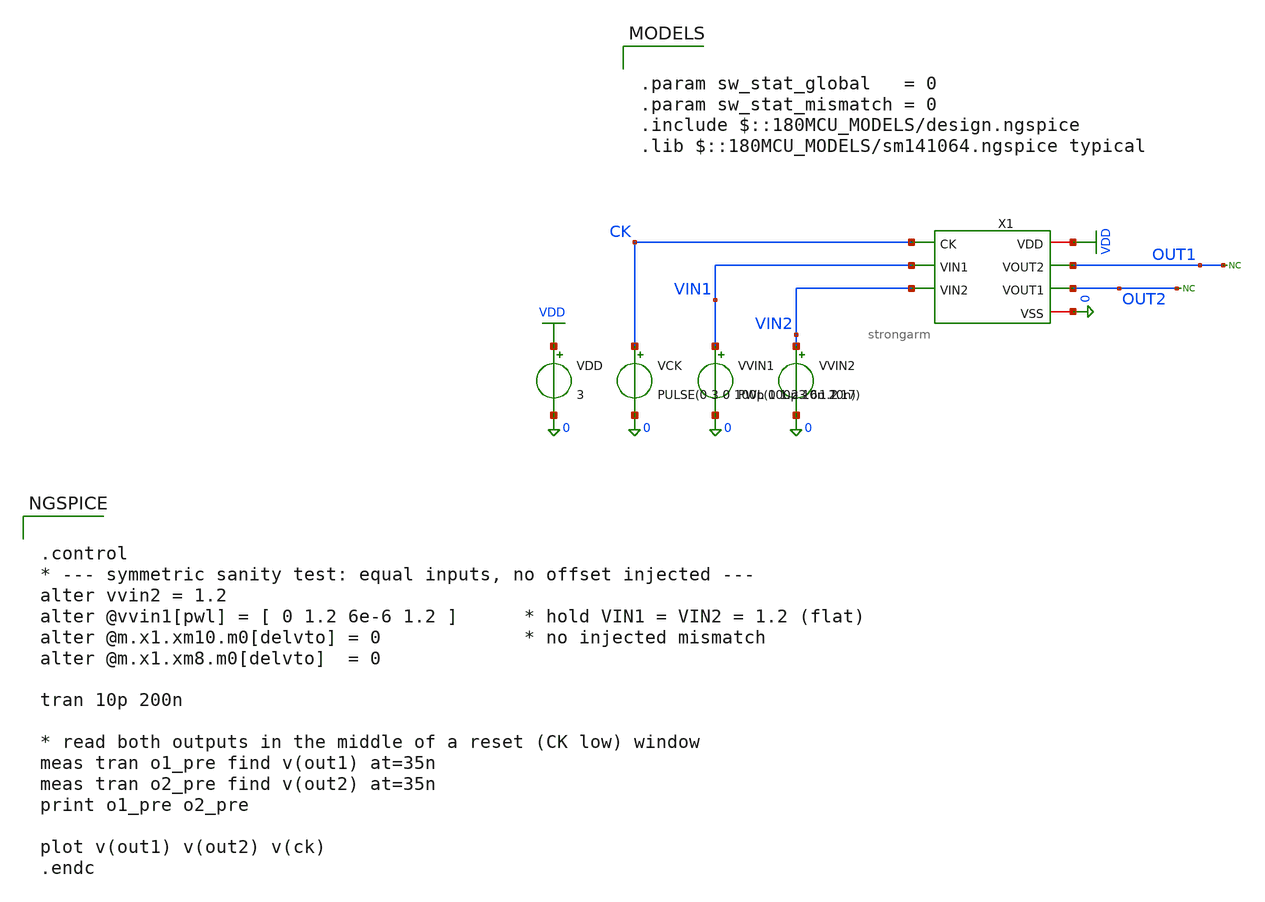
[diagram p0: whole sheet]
** sch_path: comparator/schematic/tests/strongarm_aysmetric_check_tb.sch
**.subckt strongarm_aysmetric_check_tb
X1 VDD CK OUT1 OUT2 VIN1 VIN2 0 strongarm
VVIN2 VIN2 0 1.2
VVIN1 VIN1 0 PWL(0 1.23 6u 1.17)
VDD VDD 0 3
VCK CK 0 PULSE(0 3 0 100p 100p 10n 20n)
* noconn OUT2
* noconn OUT1
**** begin user architecture code

.param sw_stat_global   = 0
.param sw_stat_mismatch = 0
.include $::180MCU_MODELS/design.ngspice
.lib $::180MCU_MODELS/sm141064.ngspice typical



.control
* --- symmetric sanity test: equal inputs, no offset injected ---
alter vvin2 = 1.2
alter @vvin1[pwl] = [ 0 1.2 6e-6 1.2 ]      * hold VIN1 = VIN2 = 1.2 (flat)
alter @m.x1.xm10.m0[delvto] = 0             * no injected mismatch
alter @m.x1.xm8.m0[delvto]  = 0

tran 10p 200n

* read both outputs in the middle of a reset (CK low) window
meas tran o1_pre find v(out1) at=35n
meas tran o2_pre find v(out2) at=35n
print o1_pre o2_pre

plot v(out1) v(out2) v(ck)
.endc


**** end user architecture code
**.ends

* expanding   symbol:  comparator/schematic/strongarm.sym # of pins=7
** sym_path: comparator/schematic/strongarm.sym
** sch_path: comparator/schematic/strongarm.sch
.subckt strongarm VDD CK VOUT2 VOUT1 VIN1 VIN2 VSS
*.opin VOUT1
*.opin VOUT2
*.ipin VIN1
*.ipin VIN2
*.ipin CK
*.iopin VDD
*.iopin VSS
XM1 VOUT2 VOUT1 net1 net1 nfet_03v3 L=0.28u W=0.22u nf=1 ad='int((nf+1)/2) * W/nf * 0.18u' as='int((nf+2)/2) * W/nf * 0.18u'
+ pd='2*int((nf+1)/2) * (W/nf + 0.18u)' ps='2*int((nf+2)/2) * (W/nf + 0.18u)' nrd='0.18u / W' nrs='0.18u / W'
+ sa=0 sb=0 sd=0 m=1
XM2 VOUT1 VOUT2 VDD VDD pfet_03v3 L=0.28u W=0.22u nf=1 ad='int((nf+1)/2) * W/nf * 0.18u' as='int((nf+2)/2) * W/nf * 0.18u'
+ pd='2*int((nf+1)/2) * (W/nf + 0.18u)' ps='2*int((nf+2)/2) * (W/nf + 0.18u)' nrd='0.18u / W' nrs='0.18u / W'
+ sa=0 sb=0 sd=0 m=1
XM3 VOUT1 CK VDD VDD pfet_03v3 L=0.28u W=0.22u nf=1 ad='int((nf+1)/2) * W/nf * 0.18u' as='int((nf+2)/2) * W/nf * 0.18u'
+ pd='2*int((nf+1)/2) * (W/nf + 0.18u)' ps='2*int((nf+2)/2) * (W/nf + 0.18u)' nrd='0.18u / W' nrs='0.18u / W'
+ sa=0 sb=0 sd=0 m=1
XM4 net3 CK VDD VDD pfet_03v3 L=0.28u W=0.22u nf=1 ad='int((nf+1)/2) * W/nf * 0.18u' as='int((nf+2)/2) * W/nf * 0.18u'
+ pd='2*int((nf+1)/2) * (W/nf + 0.18u)' ps='2*int((nf+2)/2) * (W/nf + 0.18u)' nrd='0.18u / W' nrs='0.18u / W'
+ sa=0 sb=0 sd=0 m=1
XM5 net1 CK VDD VDD pfet_03v3 L=0.28u W=0.22u nf=1 ad='int((nf+1)/2) * W/nf * 0.18u' as='int((nf+2)/2) * W/nf * 0.18u'
+ pd='2*int((nf+1)/2) * (W/nf + 0.18u)' ps='2*int((nf+2)/2) * (W/nf + 0.18u)' nrd='0.18u / W' nrs='0.18u / W'
+ sa=0 sb=0 sd=0 m=1
XM6 VOUT2 CK VDD VDD pfet_03v3 L=0.28u W=0.22u nf=1 ad='int((nf+1)/2) * W/nf * 0.18u' as='int((nf+2)/2) * W/nf * 0.18u'
+ pd='2*int((nf+1)/2) * (W/nf + 0.18u)' ps='2*int((nf+2)/2) * (W/nf + 0.18u)' nrd='0.18u / W' nrs='0.18u / W'
+ sa=0 sb=0 sd=0 m=1
XM7 VOUT2 VOUT1 VDD VDD pfet_03v3 L=0.28u W=0.22u nf=1 ad='int((nf+1)/2) * W/nf * 0.18u' as='int((nf+2)/2) * W/nf * 0.18u'
+ pd='2*int((nf+1)/2) * (W/nf + 0.18u)' ps='2*int((nf+2)/2) * (W/nf + 0.18u)' nrd='0.18u / W' nrs='0.18u / W'
+ sa=0 sb=0 sd=0 m=1
XM8 net1 VIN2 net2 net2 nfet_03v3 L=0.28u W=0.22u nf=1 ad='int((nf+1)/2) * W/nf * 0.18u' as='int((nf+2)/2) * W/nf * 0.18u'
+ pd='2*int((nf+1)/2) * (W/nf + 0.18u)' ps='2*int((nf+2)/2) * (W/nf + 0.18u)' nrd='0.18u / W' nrs='0.18u / W'
+ sa=0 sb=0 sd=0 m=1
XM9 VOUT1 VOUT2 net3 net3 nfet_03v3 L=0.28u W=0.22u nf=1 ad='int((nf+1)/2) * W/nf * 0.18u' as='int((nf+2)/2) * W/nf * 0.18u'
+ pd='2*int((nf+1)/2) * (W/nf + 0.18u)' ps='2*int((nf+2)/2) * (W/nf + 0.18u)' nrd='0.18u / W' nrs='0.18u / W'
+ sa=0 sb=0 sd=0 m=1
XM10 net3 VIN1 net2 net2 nfet_03v3 L=0.28u W=0.22u nf=1 ad='int((nf+1)/2) * W/nf * 0.18u' as='int((nf+2)/2) * W/nf * 0.18u'
+ pd='2*int((nf+1)/2) * (W/nf + 0.18u)' ps='2*int((nf+2)/2) * (W/nf + 0.18u)' nrd='0.18u / W' nrs='0.18u / W'
+ sa=0 sb=0 sd=0 m=1
XM11 net2 CK VSS net2 nfet_03v3 L=0.28u W=0.22u nf=1 ad='int((nf+1)/2) * W/nf * 0.18u' as='int((nf+2)/2) * W/nf * 0.18u'
+ pd='2*int((nf+1)/2) * (W/nf + 0.18u)' ps='2*int((nf+2)/2) * (W/nf + 0.18u)' nrd='0.18u / W' nrs='0.18u / W'
+ sa=0 sb=0 sd=0 m=1
.ends

.GLOBAL VDD
.end
